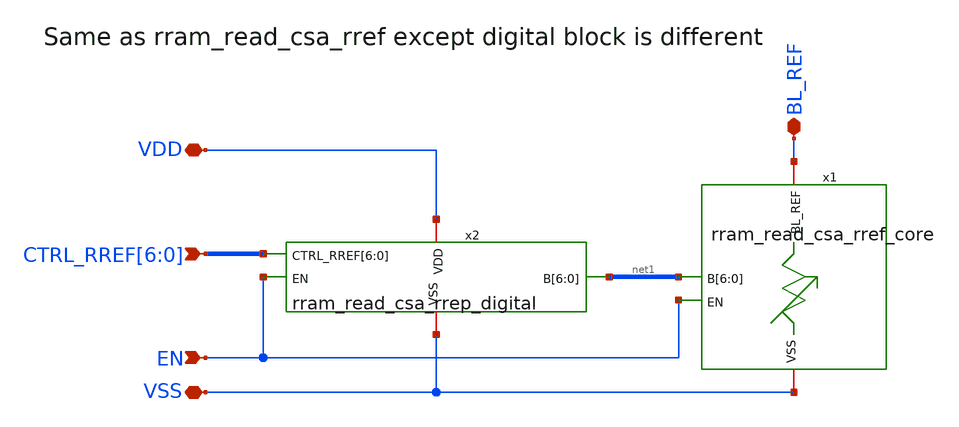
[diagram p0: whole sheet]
** sch_path: BL_Read_Interface/rram_read_csa_rrep.sch
**.subckt rram_read_csa_rrep VDD VSS EN
*+ CTRL_RREF[6],CTRL_RREF[5],CTRL_RREF[4],CTRL_RREF[3],CTRL_RREF[2],CTRL_RREF[1],CTRL_RREF[0] BL_REF
*.iopin VDD
*.iopin VSS
*.ipin EN
*.ipin CTRL_RREF[6],CTRL_RREF[5],CTRL_RREF[4],CTRL_RREF[3],CTRL_RREF[2],CTRL_RREF[1],CTRL_RREF[0]
*.iopin BL_REF
x1 BL_REF net1[6] net1[5] net1[4] net1[3] net1[2] net1[1] net1[0] EN VSS rram_read_csa_rref_core
x2 VDD CTRL_RREF[6] CTRL_RREF[5] CTRL_RREF[4] CTRL_RREF[3] CTRL_RREF[2] CTRL_RREF[1] CTRL_RREF[0]
+ net1[6] net1[5] net1[4] net1[3] net1[2] net1[1] net1[0] EN VSS rram_read_csa_rrep_digital
**.ends

* expanding   symbol:  rram_read_csa_rref_core.sym # of pins=4
** sym_path: BL_Read_Interface/rram_read_csa_rref_core.sym
** sch_path: BL_Read_Interface/rram_read_csa_rref_core.sch
.subckt rram_read_csa_rref_core BL_REF B[6] B[5] B[4] B[3] B[2] B[1] B[0] EN VSS
*.iopin VSS
*.iopin BL_REF
*.ipin B[6],B[5],B[4],B[3],B[2],B[1],B[0]
*.ipin EN
XR0d net1 BL_REF VSS sky130_fd_pr__res_xhigh_po W=0.33 L=8*5 mult=1 m=1
XR0 net8 BL_REF VSS sky130_fd_pr__res_xhigh_po W=0.33 L=8*5 mult=1 m=1
XR1 net2 BL_REF VSS sky130_fd_pr__res_xhigh_po W=0.33 L=4*5 mult=1 m=1
XR2 net3 BL_REF VSS sky130_fd_pr__res_xhigh_po W=0.33 L=2*5 mult=1 m=1
XR3 net4 BL_REF VSS sky130_fd_pr__res_xhigh_po W=0.33 L=1*5 mult=1 m=1
XR4[1] net5[1] BL_REF VSS sky130_fd_pr__res_xhigh_po W=0.33 L=1*5 mult=1 m=1
XR4[0] net5[0] BL_REF VSS sky130_fd_pr__res_xhigh_po W=0.33 L=1*5 mult=1 m=1
XR5[3] net6[3] BL_REF VSS sky130_fd_pr__res_xhigh_po W=0.33 L=1*5 mult=1 m=1
XR5[2] net6[2] BL_REF VSS sky130_fd_pr__res_xhigh_po W=0.33 L=1*5 mult=1 m=1
XR5[1] net6[1] BL_REF VSS sky130_fd_pr__res_xhigh_po W=0.33 L=1*5 mult=1 m=1
XR5[0] net6[0] BL_REF VSS sky130_fd_pr__res_xhigh_po W=0.33 L=1*5 mult=1 m=1
XR6[7] net7[7] BL_REF VSS sky130_fd_pr__res_xhigh_po W=0.33 L=1*5 mult=1 m=1
XR6[6] net7[6] BL_REF VSS sky130_fd_pr__res_xhigh_po W=0.33 L=1*5 mult=1 m=1
XR6[5] net7[5] BL_REF VSS sky130_fd_pr__res_xhigh_po W=0.33 L=1*5 mult=1 m=1
XR6[4] net7[4] BL_REF VSS sky130_fd_pr__res_xhigh_po W=0.33 L=1*5 mult=1 m=1
XR6[3] net7[3] BL_REF VSS sky130_fd_pr__res_xhigh_po W=0.33 L=1*5 mult=1 m=1
XR6[2] net7[2] BL_REF VSS sky130_fd_pr__res_xhigh_po W=0.33 L=1*5 mult=1 m=1
XR6[1] net7[1] BL_REF VSS sky130_fd_pr__res_xhigh_po W=0.33 L=1*5 mult=1 m=1
XR6[0] net7[0] BL_REF VSS sky130_fd_pr__res_xhigh_po W=0.33 L=1*5 mult=1 m=1
XMN0d net1 EN VSS VSS sky130_fd_pr__nfet_01v8 L=0.15 W=0.42 nf=1 ad='int((nf+1)/2) * W/nf * 0.29' as='int((nf+2)/2) * W/nf * 0.29'
+ pd='2*int((nf+1)/2) * (W/nf + 0.29)' ps='2*int((nf+2)/2) * (W/nf + 0.29)' nrd='0.29 / W' nrs='0.29 / W'
+ sa=0 sb=0 sd=0 mult=1 m=1
XMN0 net8 B[0] VSS VSS sky130_fd_pr__nfet_01v8 L=0.15 W=0.42 nf=1 ad='int((nf+1)/2) * W/nf * 0.29' as='int((nf+2)/2) * W/nf * 0.29'
+ pd='2*int((nf+1)/2) * (W/nf + 0.29)' ps='2*int((nf+2)/2) * (W/nf + 0.29)' nrd='0.29 / W' nrs='0.29 / W'
+ sa=0 sb=0 sd=0 mult=1 m=1
XMN1 net2 B[1] VSS VSS sky130_fd_pr__nfet_01v8 L=0.15 W=0.42 nf=1 ad='int((nf+1)/2) * W/nf * 0.29' as='int((nf+2)/2) * W/nf * 0.29'
+ pd='2*int((nf+1)/2) * (W/nf + 0.29)' ps='2*int((nf+2)/2) * (W/nf + 0.29)' nrd='0.29 / W' nrs='0.29 / W'
+ sa=0 sb=0 sd=0 mult=1 m=1
XMN2 net3 B[2] VSS VSS sky130_fd_pr__nfet_01v8 L=0.15 W=0.58 nf=1 ad='int((nf+1)/2) * W/nf * 0.29' as='int((nf+2)/2) * W/nf * 0.29'
+ pd='2*int((nf+1)/2) * (W/nf + 0.29)' ps='2*int((nf+2)/2) * (W/nf + 0.29)' nrd='0.29 / W' nrs='0.29 / W'
+ sa=0 sb=0 sd=0 mult=1 m=1
XMN3 net4 B[3] VSS VSS sky130_fd_pr__nfet_01v8 L=0.15 W=1 nf=1 ad='int((nf+1)/2) * W/nf * 0.29' as='int((nf+2)/2) * W/nf * 0.29'
+ pd='2*int((nf+1)/2) * (W/nf + 0.29)' ps='2*int((nf+2)/2) * (W/nf + 0.29)' nrd='0.29 / W' nrs='0.29 / W'
+ sa=0 sb=0 sd=0 mult=1 m=1
XMN4[1] net5[1] B[4] VSS VSS sky130_fd_pr__nfet_01v8 L=0.15 W=1 nf=1 ad='int((nf+1)/2) * W/nf * 0.29'
+ as='int((nf+2)/2) * W/nf * 0.29' pd='2*int((nf+1)/2) * (W/nf + 0.29)' ps='2*int((nf+2)/2) * (W/nf + 0.29)'
+ nrd='0.29 / W' nrs='0.29 / W' sa=0 sb=0 sd=0 mult=1 m=1
XMN4[0] net5[0] B[4] VSS VSS sky130_fd_pr__nfet_01v8 L=0.15 W=1 nf=1 ad='int((nf+1)/2) * W/nf * 0.29'
+ as='int((nf+2)/2) * W/nf * 0.29' pd='2*int((nf+1)/2) * (W/nf + 0.29)' ps='2*int((nf+2)/2) * (W/nf + 0.29)'
+ nrd='0.29 / W' nrs='0.29 / W' sa=0 sb=0 sd=0 mult=1 m=1
XMN5[3] net6[3] B[5] VSS VSS sky130_fd_pr__nfet_01v8 L=0.15 W=1 nf=1 ad='int((nf+1)/2) * W/nf * 0.29'
+ as='int((nf+2)/2) * W/nf * 0.29' pd='2*int((nf+1)/2) * (W/nf + 0.29)' ps='2*int((nf+2)/2) * (W/nf + 0.29)'
+ nrd='0.29 / W' nrs='0.29 / W' sa=0 sb=0 sd=0 mult=1 m=1
XMN5[2] net6[2] B[5] VSS VSS sky130_fd_pr__nfet_01v8 L=0.15 W=1 nf=1 ad='int((nf+1)/2) * W/nf * 0.29'
+ as='int((nf+2)/2) * W/nf * 0.29' pd='2*int((nf+1)/2) * (W/nf + 0.29)' ps='2*int((nf+2)/2) * (W/nf + 0.29)'
+ nrd='0.29 / W' nrs='0.29 / W' sa=0 sb=0 sd=0 mult=1 m=1
XMN5[1] net6[1] B[5] VSS VSS sky130_fd_pr__nfet_01v8 L=0.15 W=1 nf=1 ad='int((nf+1)/2) * W/nf * 0.29'
+ as='int((nf+2)/2) * W/nf * 0.29' pd='2*int((nf+1)/2) * (W/nf + 0.29)' ps='2*int((nf+2)/2) * (W/nf + 0.29)'
+ nrd='0.29 / W' nrs='0.29 / W' sa=0 sb=0 sd=0 mult=1 m=1
XMN5[0] net6[0] B[5] VSS VSS sky130_fd_pr__nfet_01v8 L=0.15 W=1 nf=1 ad='int((nf+1)/2) * W/nf * 0.29'
+ as='int((nf+2)/2) * W/nf * 0.29' pd='2*int((nf+1)/2) * (W/nf + 0.29)' ps='2*int((nf+2)/2) * (W/nf + 0.29)'
+ nrd='0.29 / W' nrs='0.29 / W' sa=0 sb=0 sd=0 mult=1 m=1
XMN6[7] net7[7] B[6] VSS VSS sky130_fd_pr__nfet_01v8 L=0.15 W=1 nf=1 ad='int((nf+1)/2) * W/nf * 0.29'
+ as='int((nf+2)/2) * W/nf * 0.29' pd='2*int((nf+1)/2) * (W/nf + 0.29)' ps='2*int((nf+2)/2) * (W/nf + 0.29)'
+ nrd='0.29 / W' nrs='0.29 / W' sa=0 sb=0 sd=0 mult=1 m=1
XMN6[6] net7[6] B[6] VSS VSS sky130_fd_pr__nfet_01v8 L=0.15 W=1 nf=1 ad='int((nf+1)/2) * W/nf * 0.29'
+ as='int((nf+2)/2) * W/nf * 0.29' pd='2*int((nf+1)/2) * (W/nf + 0.29)' ps='2*int((nf+2)/2) * (W/nf + 0.29)'
+ nrd='0.29 / W' nrs='0.29 / W' sa=0 sb=0 sd=0 mult=1 m=1
XMN6[5] net7[5] B[6] VSS VSS sky130_fd_pr__nfet_01v8 L=0.15 W=1 nf=1 ad='int((nf+1)/2) * W/nf * 0.29'
+ as='int((nf+2)/2) * W/nf * 0.29' pd='2*int((nf+1)/2) * (W/nf + 0.29)' ps='2*int((nf+2)/2) * (W/nf + 0.29)'
+ nrd='0.29 / W' nrs='0.29 / W' sa=0 sb=0 sd=0 mult=1 m=1
XMN6[4] net7[4] B[6] VSS VSS sky130_fd_pr__nfet_01v8 L=0.15 W=1 nf=1 ad='int((nf+1)/2) * W/nf * 0.29'
+ as='int((nf+2)/2) * W/nf * 0.29' pd='2*int((nf+1)/2) * (W/nf + 0.29)' ps='2*int((nf+2)/2) * (W/nf + 0.29)'
+ nrd='0.29 / W' nrs='0.29 / W' sa=0 sb=0 sd=0 mult=1 m=1
XMN6[3] net7[3] B[6] VSS VSS sky130_fd_pr__nfet_01v8 L=0.15 W=1 nf=1 ad='int((nf+1)/2) * W/nf * 0.29'
+ as='int((nf+2)/2) * W/nf * 0.29' pd='2*int((nf+1)/2) * (W/nf + 0.29)' ps='2*int((nf+2)/2) * (W/nf + 0.29)'
+ nrd='0.29 / W' nrs='0.29 / W' sa=0 sb=0 sd=0 mult=1 m=1
XMN6[2] net7[2] B[6] VSS VSS sky130_fd_pr__nfet_01v8 L=0.15 W=1 nf=1 ad='int((nf+1)/2) * W/nf * 0.29'
+ as='int((nf+2)/2) * W/nf * 0.29' pd='2*int((nf+1)/2) * (W/nf + 0.29)' ps='2*int((nf+2)/2) * (W/nf + 0.29)'
+ nrd='0.29 / W' nrs='0.29 / W' sa=0 sb=0 sd=0 mult=1 m=1
XMN6[1] net7[1] B[6] VSS VSS sky130_fd_pr__nfet_01v8 L=0.15 W=1 nf=1 ad='int((nf+1)/2) * W/nf * 0.29'
+ as='int((nf+2)/2) * W/nf * 0.29' pd='2*int((nf+1)/2) * (W/nf + 0.29)' ps='2*int((nf+2)/2) * (W/nf + 0.29)'
+ nrd='0.29 / W' nrs='0.29 / W' sa=0 sb=0 sd=0 mult=1 m=1
XMN6[0] net7[0] B[6] VSS VSS sky130_fd_pr__nfet_01v8 L=0.15 W=1 nf=1 ad='int((nf+1)/2) * W/nf * 0.29'
+ as='int((nf+2)/2) * W/nf * 0.29' pd='2*int((nf+1)/2) * (W/nf + 0.29)' ps='2*int((nf+2)/2) * (W/nf + 0.29)'
+ nrd='0.29 / W' nrs='0.29 / W' sa=0 sb=0 sd=0 mult=1 m=1
.ends


* expanding   symbol:  rram_read_csa_rrep_digital.sym # of pins=5
** sym_path: BL_Read_Interface/rram_read_csa_rrep_digital.sym
** sch_path: BL_Read_Interface/rram_read_csa_rrep_digital.sch
.subckt rram_read_csa_rrep_digital VDD CTRL_RREF[6] CTRL_RREF[5] CTRL_RREF[4] CTRL_RREF[3]
+ CTRL_RREF[2] CTRL_RREF[1] CTRL_RREF[0] B[6] B[5] B[4] B[3] B[2] B[1] B[0] EN VSS
*.iopin VSS
*.iopin VDD
*.ipin CTRL_RREF[6],CTRL_RREF[5],CTRL_RREF[4],CTRL_RREF[3],CTRL_RREF[2],CTRL_RREF[1],CTRL_RREF[0]
*.ipin EN
*.opin B[6],B[5],B[4],B[3],B[2],B[1],B[0]
xinv[6] CTRL_RREF[6] VSS VSS VDD VDD RREFB[6] sky130_fd_sc_hd__inv_1
xinv[5] CTRL_RREF[5] VSS VSS VDD VDD RREFB[5] sky130_fd_sc_hd__inv_1
xinv[4] CTRL_RREF[4] VSS VSS VDD VDD RREFB[4] sky130_fd_sc_hd__inv_1
xinv[3] CTRL_RREF[3] VSS VSS VDD VDD RREFB[3] sky130_fd_sc_hd__inv_1
xinv[2] CTRL_RREF[2] VSS VSS VDD VDD RREFB[2] sky130_fd_sc_hd__inv_1
xinv[1] CTRL_RREF[1] VSS VSS VDD VDD RREFB[1] sky130_fd_sc_hd__inv_1
xinv[0] CTRL_RREF[0] VSS VSS VDD VDD RREFB[0] sky130_fd_sc_hd__inv_1
x1 RREFB[6] RREFB[5] RREFB[4] VSS VSS VDD VDD net2 sky130_fd_sc_hd__nand3_1
x2 RREFB[3] RREFB[2] RREFB[1] VSS VSS VDD VDD net1 sky130_fd_sc_hd__nand3_1
x3 net2 net1 VSS VSS VDD VDD CLIP_LOW sky130_fd_sc_hd__nor2_1
xinv1 CLIP_LOW VSS VSS VDD VDD CLIP_LOWB sky130_fd_sc_hd__inv_1
xinv2 EN VSS VSS VDD VDD ENB sky130_fd_sc_hd__inv_1
x4 RREFB[1] CLIP_LOWB VSS VSS VDD VDD RREF_CLIP[1] sky130_fd_sc_hd__and2_1
x5 RREFB[0] CLIP_LOW VSS VSS VDD VDD RREF_CLIP[0] sky130_fd_sc_hd__or2_1
x6[6] RREFB[6] ENB VSS VSS VDD VDD B[6] sky130_fd_sc_hd__or2_1
x6[5] RREFB[5] ENB VSS VSS VDD VDD B[5] sky130_fd_sc_hd__or2_1
x6[4] RREFB[4] ENB VSS VSS VDD VDD B[4] sky130_fd_sc_hd__or2_1
x6[3] RREFB[3] ENB VSS VSS VDD VDD B[3] sky130_fd_sc_hd__or2_1
x6[2] RREFB[2] ENB VSS VSS VDD VDD B[2] sky130_fd_sc_hd__or2_1
x6[1] RREF_CLIP[1] ENB VSS VSS VDD VDD B[1] sky130_fd_sc_hd__or2_1
x6[0] RREF_CLIP[0] ENB VSS VSS VDD VDD B[0] sky130_fd_sc_hd__or2_1
.ends

.end
